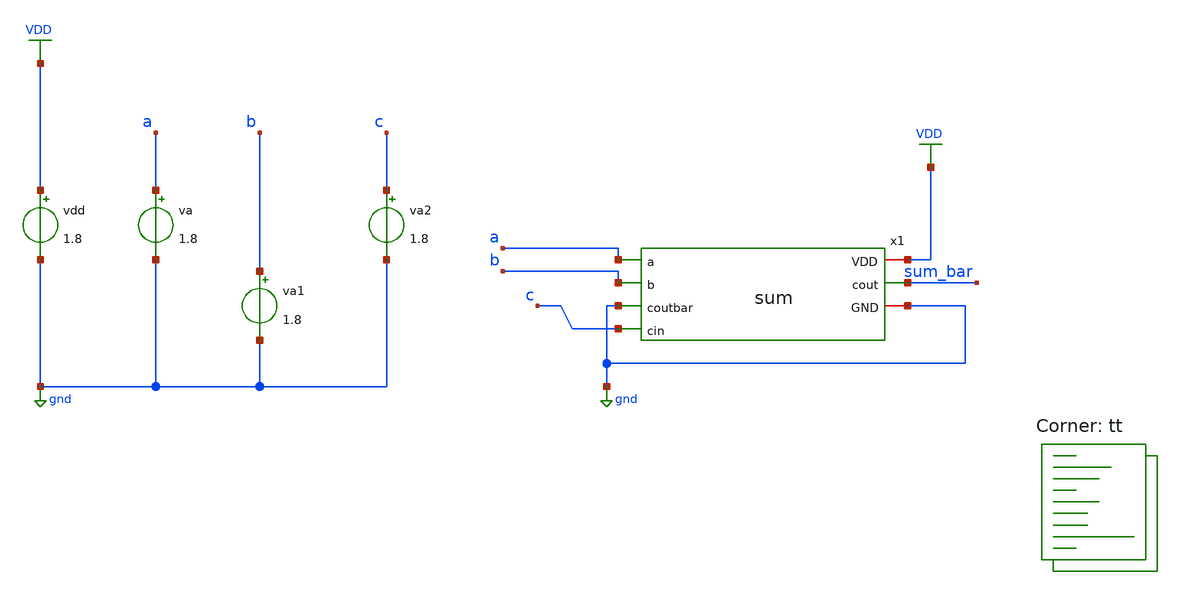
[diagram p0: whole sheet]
** sch_path: assignments/assignment7/sum_tb.sch
**.subckt sum_tb
x1 VDD a b gnd c sum_bar gnd sum
vdd VDD gnd 1.8
va a gnd 1.8
va1 b gnd 1.8
va2 c gnd 1.8
**** begin user architecture code


.control
alter @va[pulse] = [ 1.8 0 10p 5p 5p]
alter @va1[pulse] = [ 1.8 0 10p 5p 5p]
alter @va2[pulse] = [ 1.8 0 10p 5p 5p]

tran 1p 400p

plot v(a) v(b) v(c) v(sum_bar)
.endc


.lib $::SKYWATER_MODELS/sky130.lib.spice tt
**** end user architecture code
**.ends

* expanding   symbol:  sum.sym # of pins=7
** sym_path: assignments/assignment7/sum.sym
** sch_path: assignments/assignment7/sum.sch
.subckt sum VDD a b coutbar cin cout GND
*.opin cout
*.ipin a
*.iopin VDD
*.iopin GND
*.ipin b
*.ipin coutbar
*.ipin cin
XM1 cout coutbar net4 GND sky130_fd_pr__nfet_01v8 L=0.15 W=0.84 nf=1 ad='int((nf+1)/2) * W/nf * 0.29'
+ as='int((nf+2)/2) * W/nf * 0.29' pd='2*int((nf+1)/2) * (W/nf + 0.29)' ps='2*int((nf+2)/2) * (W/nf + 0.29)'
+ nrd='0.29 / W' nrs='0.29 / W' sa=0 sb=0 sd=0 mult=1 m=1
XM2 net1 b VDD VDD sky130_fd_pr__pfet_01v8 L=0.15 W=1.68 nf=1 ad='int((nf+1)/2) * W/nf * 0.29' as='int((nf+2)/2) * W/nf * 0.29'
+ pd='2*int((nf+1)/2) * (W/nf + 0.29)' ps='2*int((nf+2)/2) * (W/nf + 0.29)' nrd='0.29 / W' nrs='0.29 / W'
+ sa=0 sb=0 sd=0 mult=1 m=1
XM4 cout coutbar net1 VDD sky130_fd_pr__pfet_01v8 L=0.15 W=1.68 nf=1 ad='int((nf+1)/2) * W/nf * 0.29'
+ as='int((nf+2)/2) * W/nf * 0.29' pd='2*int((nf+1)/2) * (W/nf + 0.29)' ps='2*int((nf+2)/2) * (W/nf + 0.29)'
+ nrd='0.29 / W' nrs='0.29 / W' sa=0 sb=0 sd=0 mult=1 m=1
XM5 net1 a VDD VDD sky130_fd_pr__pfet_01v8 L=0.15 W=1.68 nf=1 ad='int((nf+1)/2) * W/nf * 0.29' as='int((nf+2)/2) * W/nf * 0.29'
+ pd='2*int((nf+1)/2) * (W/nf + 0.29)' ps='2*int((nf+2)/2) * (W/nf + 0.29)' nrd='0.29 / W' nrs='0.29 / W'
+ sa=0 sb=0 sd=0 mult=1 m=1
XM6 net1 cin VDD VDD sky130_fd_pr__pfet_01v8 L=0.15 W=1.68 nf=1 ad='int((nf+1)/2) * W/nf * 0.29' as='int((nf+2)/2) * W/nf * 0.29'
+ pd='2*int((nf+1)/2) * (W/nf + 0.29)' ps='2*int((nf+2)/2) * (W/nf + 0.29)' nrd='0.29 / W' nrs='0.29 / W'
+ sa=0 sb=0 sd=0 mult=1 m=1
XM7 net3 a VDD VDD sky130_fd_pr__pfet_01v8 L=0.15 W=1.68 nf=1 ad='int((nf+1)/2) * W/nf * 0.29' as='int((nf+2)/2) * W/nf * 0.29'
+ pd='2*int((nf+1)/2) * (W/nf + 0.29)' ps='2*int((nf+2)/2) * (W/nf + 0.29)' nrd='0.29 / W' nrs='0.29 / W'
+ sa=0 sb=0 sd=0 mult=1 m=1
XM3 net2 b net3 VDD sky130_fd_pr__pfet_01v8 L=0.15 W=1.68 nf=1 ad='int((nf+1)/2) * W/nf * 0.29' as='int((nf+2)/2) * W/nf * 0.29'
+ pd='2*int((nf+1)/2) * (W/nf + 0.29)' ps='2*int((nf+2)/2) * (W/nf + 0.29)' nrd='0.29 / W' nrs='0.29 / W'
+ sa=0 sb=0 sd=0 mult=1 m=1
XM8 cout cin net2 VDD sky130_fd_pr__pfet_01v8 L=0.15 W=1.68 nf=1 ad='int((nf+1)/2) * W/nf * 0.29' as='int((nf+2)/2) * W/nf * 0.29'
+ pd='2*int((nf+1)/2) * (W/nf + 0.29)' ps='2*int((nf+2)/2) * (W/nf + 0.29)' nrd='0.29 / W' nrs='0.29 / W'
+ sa=0 sb=0 sd=0 mult=1 m=1
XM9 net4 a GND GND sky130_fd_pr__nfet_01v8 L=0.15 W=0.84 nf=1 ad='int((nf+1)/2) * W/nf * 0.29' as='int((nf+2)/2) * W/nf * 0.29'
+ pd='2*int((nf+1)/2) * (W/nf + 0.29)' ps='2*int((nf+2)/2) * (W/nf + 0.29)' nrd='0.29 / W' nrs='0.29 / W'
+ sa=0 sb=0 sd=0 mult=1 m=1
XM10 net4 b GND GND sky130_fd_pr__nfet_01v8 L=0.15 W=0.84 nf=1 ad='int((nf+1)/2) * W/nf * 0.29' as='int((nf+2)/2) * W/nf * 0.29'
+ pd='2*int((nf+1)/2) * (W/nf + 0.29)' ps='2*int((nf+2)/2) * (W/nf + 0.29)' nrd='0.29 / W' nrs='0.29 / W'
+ sa=0 sb=0 sd=0 mult=1 m=1
XM11 net4 cin GND GND sky130_fd_pr__nfet_01v8 L=0.15 W=0.84 nf=1 ad='int((nf+1)/2) * W/nf * 0.29' as='int((nf+2)/2) * W/nf * 0.29'
+ pd='2*int((nf+1)/2) * (W/nf + 0.29)' ps='2*int((nf+2)/2) * (W/nf + 0.29)' nrd='0.29 / W' nrs='0.29 / W'
+ sa=0 sb=0 sd=0 mult=1 m=1
XM12 cout cin net6 GND sky130_fd_pr__nfet_01v8 L=0.15 W=0.84 nf=1 ad='int((nf+1)/2) * W/nf * 0.29' as='int((nf+2)/2) * W/nf * 0.29'
+ pd='2*int((nf+1)/2) * (W/nf + 0.29)' ps='2*int((nf+2)/2) * (W/nf + 0.29)' nrd='0.29 / W' nrs='0.29 / W'
+ sa=0 sb=0 sd=0 mult=1 m=1
XM13 net6 b net5 GND sky130_fd_pr__nfet_01v8 L=0.15 W=0.84 nf=1 ad='int((nf+1)/2) * W/nf * 0.29' as='int((nf+2)/2) * W/nf * 0.29'
+ pd='2*int((nf+1)/2) * (W/nf + 0.29)' ps='2*int((nf+2)/2) * (W/nf + 0.29)' nrd='0.29 / W' nrs='0.29 / W'
+ sa=0 sb=0 sd=0 mult=1 m=1
XM14 net5 a GND GND sky130_fd_pr__nfet_01v8 L=0.15 W=0.84 nf=1 ad='int((nf+1)/2) * W/nf * 0.29' as='int((nf+2)/2) * W/nf * 0.29'
+ pd='2*int((nf+1)/2) * (W/nf + 0.29)' ps='2*int((nf+2)/2) * (W/nf + 0.29)' nrd='0.29 / W' nrs='0.29 / W'
+ sa=0 sb=0 sd=0 mult=1 m=1
.ends

.GLOBAL VDD
.GLOBAL gnd
.end
